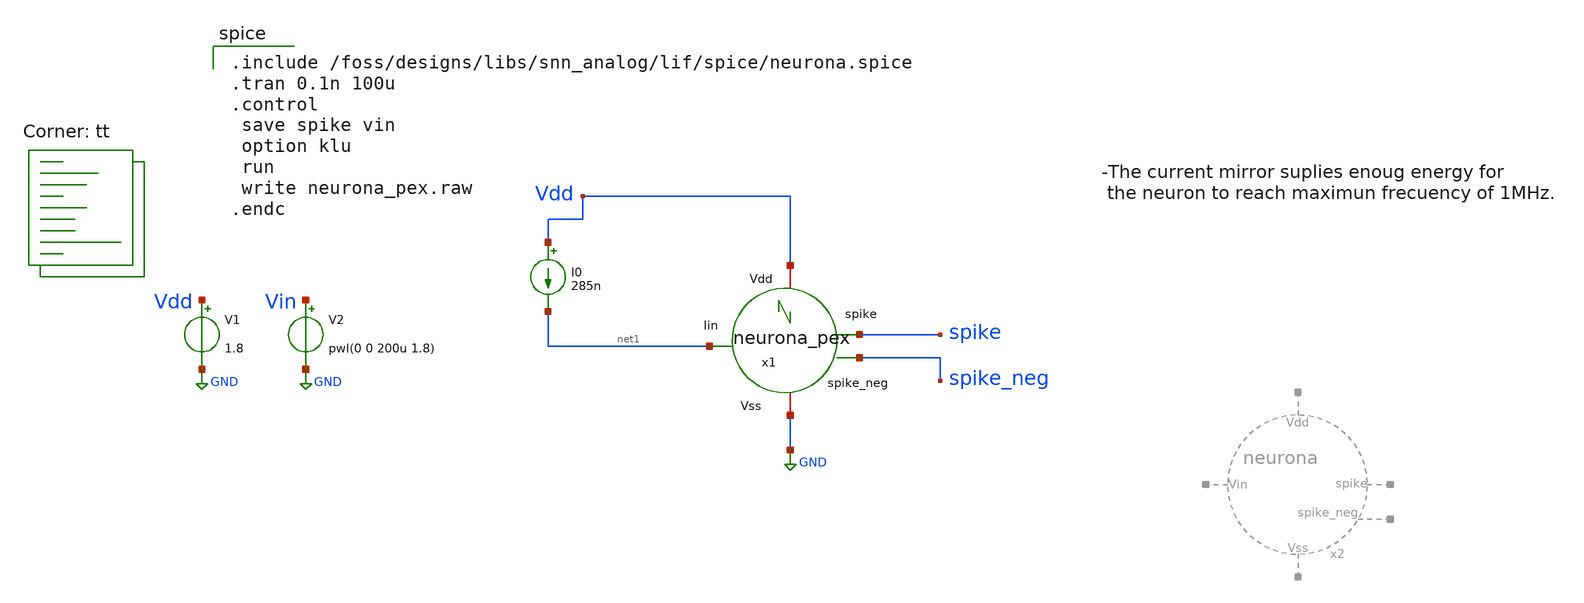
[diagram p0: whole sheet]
** sch_path: designs/libs/snn_analog/lif/sch/neurona_tb.sch
**.subckt neurona_tb
V1 Vdd GND 1.8
V2 Vin GND pwl(0 0 200u 1.8)
I0 Vdd net1 285n
x1 net1 Vdd GND spike spike_neg neurona_pex
**** begin user architecture code

.include /foss/designs/libs/snn_analog/lif/spice/neurona.spice
.tran 0.1n 100u
.control
 save spike vin
 option klu
 run
 write neurona_pex.raw
.endc

.lib $::SKYWATER_MODELS/sky130.lib.spice tt
**** end user architecture code
**.ends
.GLOBAL GND
.end
